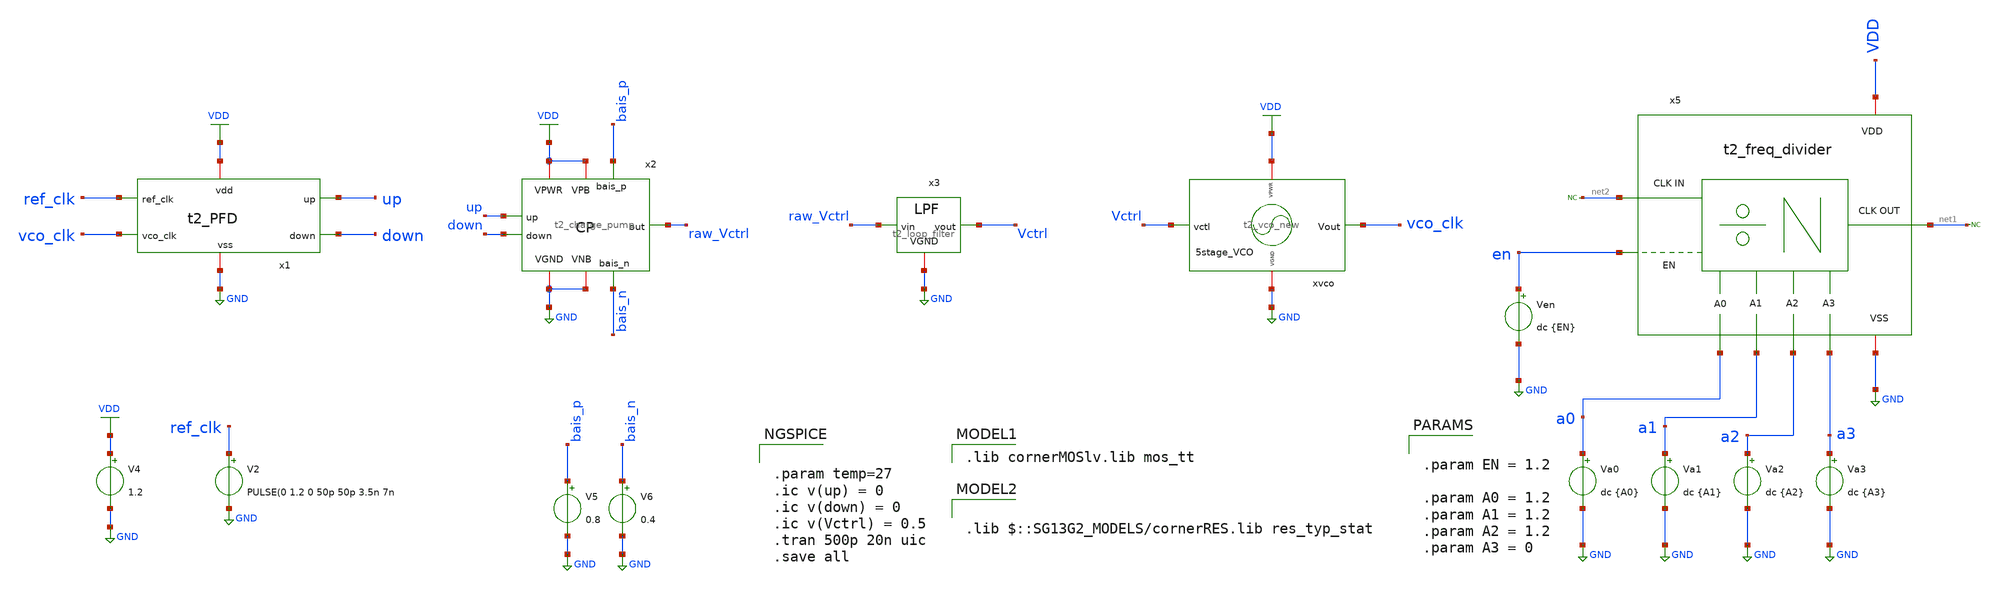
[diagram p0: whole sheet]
** sch_path: Team 2 Design/design_data/xschem/t2_pll.sch
**.subckt t2_pll
x1 VDD up GND down ref_clk vco_clk t2_PFD
V2 ref_clk GND PULSE(0 1.2 0 50p 50p 3.5n 7n
V4 VDD GND 1.2
V5 bais_p GND 0.8
V6 bais_n GND 0.4
x2 VDD VDD GND GND raw_Vctrl up down bais_p bais_n t2_charge_pump
x4 VDD GND Vctrl vco_clk t2_vco_new
x5 VDD GND net2 en a0 a1 a2 a3 net1 t2_freq_divider
Ven en GND dc {EN}
Va0 a0 GND dc {A0}
Va1 a1 GND dc {A1}
Va2 a2 GND dc {A2}
Va3 a3 GND dc {A3}
x3 GND Vctrl raw_Vctrl t2_loop_filter
* noconn #net2
* noconn #net1
**** begin user architecture code


.param EN = 1.2

.param A0 = 1.2
.param A1 = 1.2
.param A2 = 1.2
.param A3 = 0


 .lib cornerMOSlv.lib mos_tt



.param temp=27
.ic v(up) = 0
.ic v(down) = 0
.ic v(Vctrl) = 0.5
.tran 500p 20n uic
.save all



.lib $::SG13G2_MODELS/cornerRES.lib res_typ_stat

**** end user architecture code
**.ends
.GLOBAL GND
.GLOBAL VDD
.end
